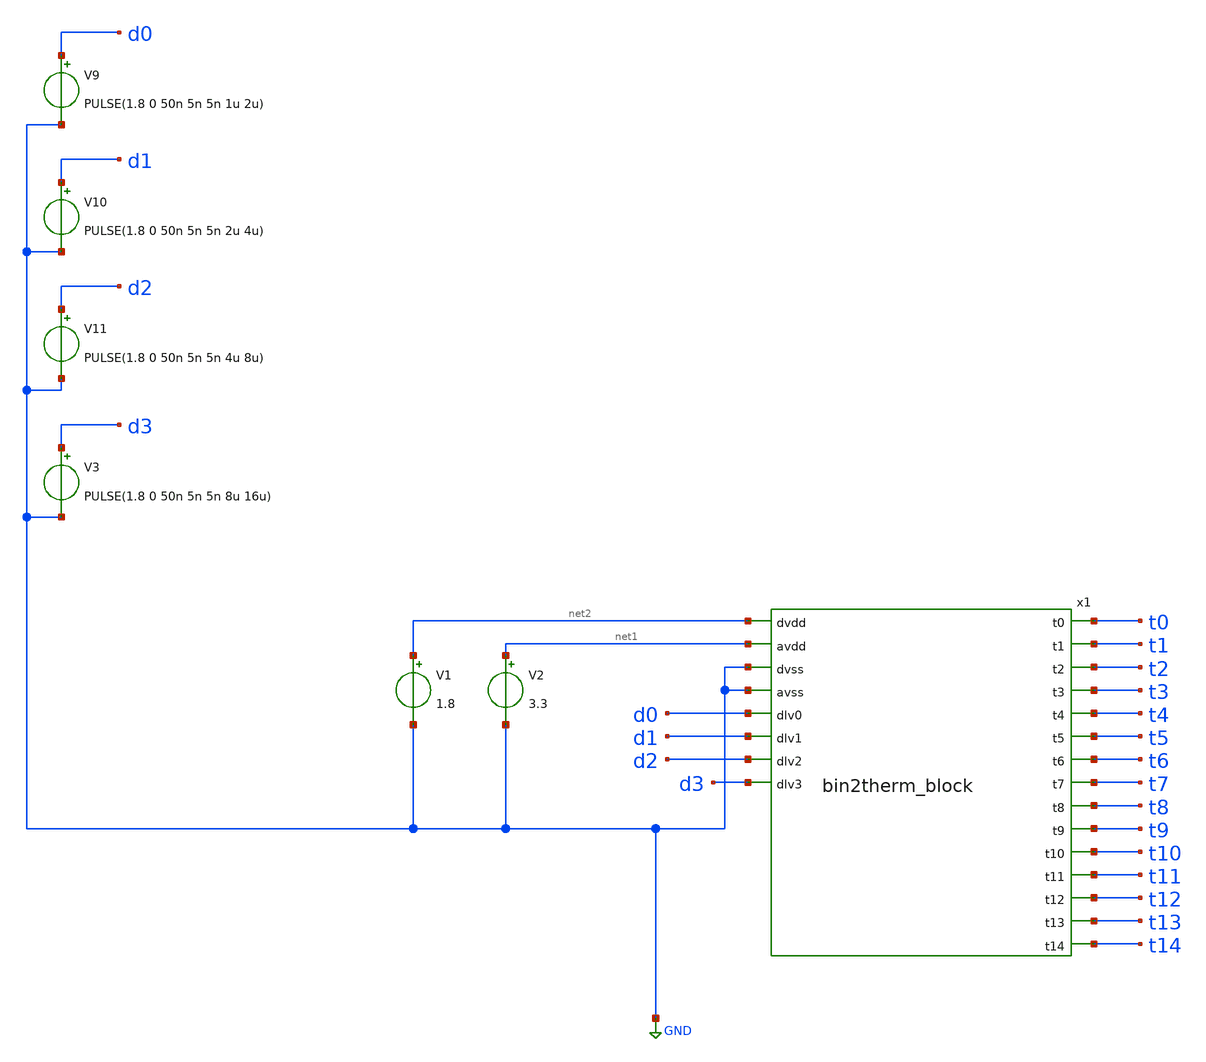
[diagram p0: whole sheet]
** sch_path: xschem/bin2thermotest_tb.sch
**.subckt bin2thermotest_tb
V1 net2 GND 1.8
V2 net1 GND 3.3
V3 d3 GND PULSE(1.8 0 50n 5n 5n 8u 16u)
V9 d0 GND PULSE(1.8 0 50n 5n 5n 1u 2u)
V10 d1 GND PULSE(1.8 0 50n 5n 5n 2u 4u)
V11 d2 GND PULSE(1.8 0 50n 5n 5n 4u 8u)
x1 net2 net1 GND GND d0 d1 d2 d3 t0 t1 t2 t3 t4 t5 t6 t7 t8 t9 t10 t11 t12 t13 t14 bin2therm_block
**** begin user architecture code
 .lib $::SKYWATER_MODELS/sky130.lib.spice tt
.include $::SKYWATER_STDCELLS/../../sky130_fd_sc_hvl/spice/sky130_fd_sc_hvl.spice

.param mc_mm_switch=0
.param mc_pr_switch=1



.option wnflag=0
.save all
.control
tran 200n 16u
plot v(t0) v(t14)
plot v(d0)
plot v(d1)
plot v(d2)
plot v(d3)
write currentmirrortb.raw v(t0) v(t1)
.endc


**** end user architecture code
**.ends
.GLOBAL GND
.end
